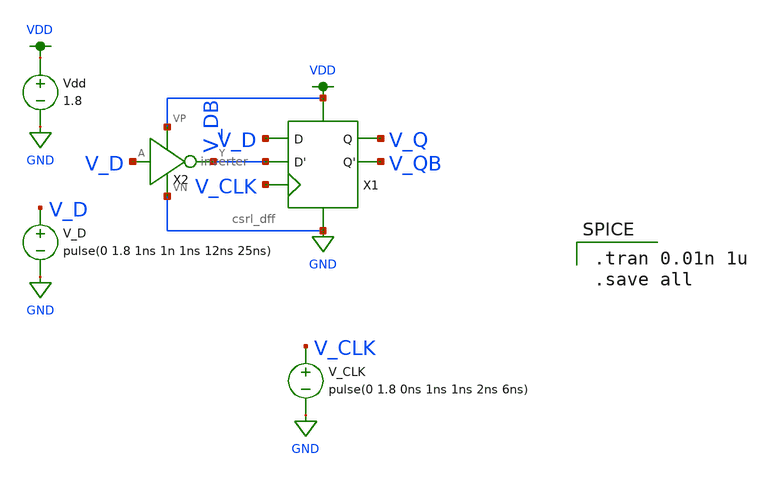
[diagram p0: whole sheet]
** sch_path: MP2/xschem/archive/csrl_dff_tran.sch
**.subckt csrl_dff_tran
Vdd VDD GND 1.8
V_D V_D GND pulse(0 1.8 1ns 1n 1ns 12ns 25ns)
V_CLK V_CLK GND pulse(0 1.8 0ns 1ns 1ns 2ns 6ns)
X2 V_D V_DB VDD GND inverter
X1 V_DB V_CLK V_D V_Q V_QB VDD GND csrl_dff
**** begin user architecture code

.tran 0.01n 1u
.save all


.option wnflag=1
.lib ~/skywater/skywater-pdk/libraries/sky130_fd_pr_ngspice/latest/models/sky130.lib.spice sf

**** end user architecture code
**.ends
.GLOBAL VDD
.GLOBAL GND
.end
